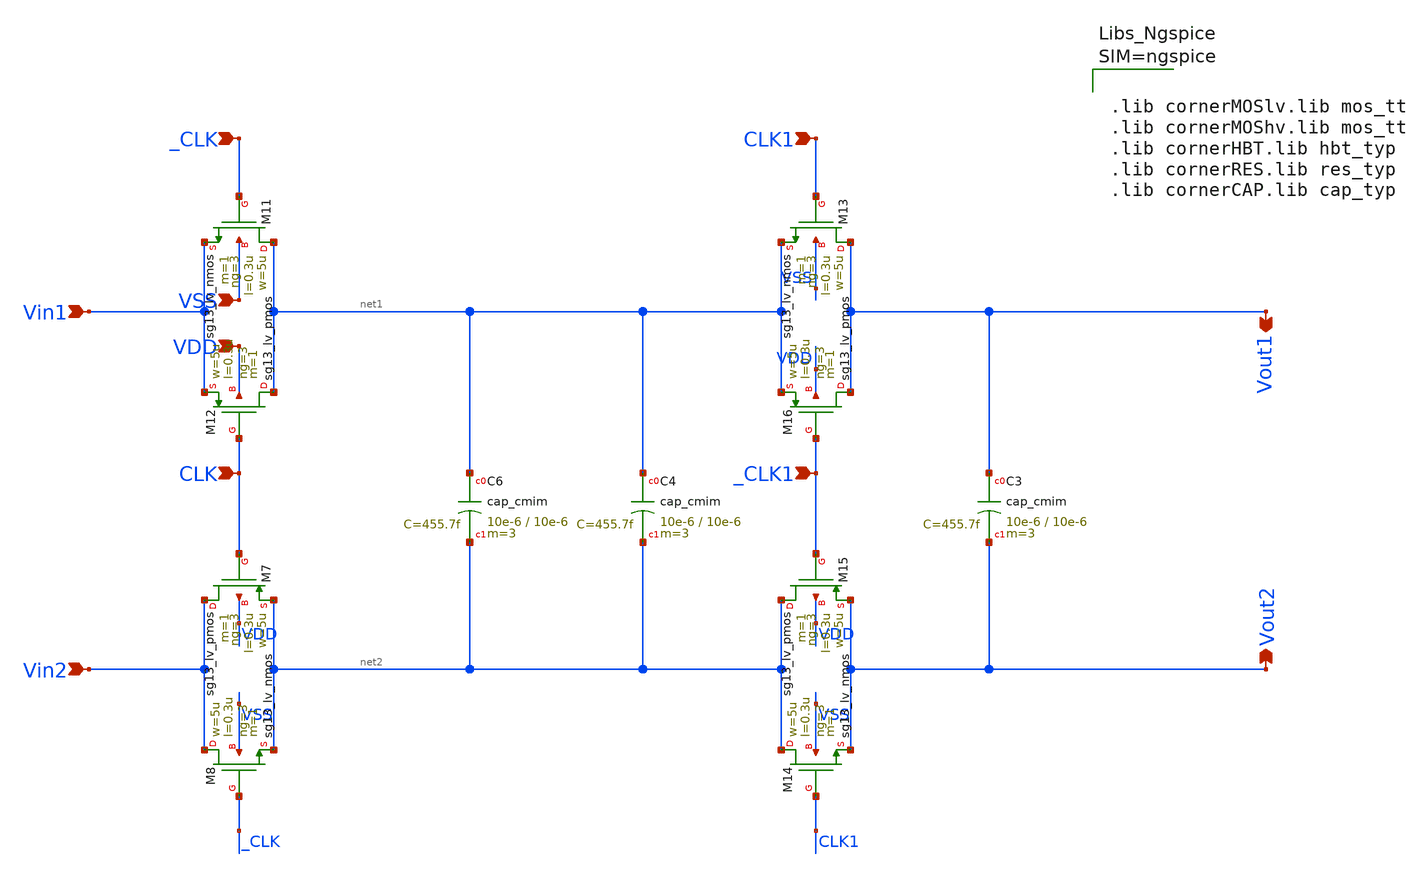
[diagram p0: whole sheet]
** sch_path: Components Progress Log/Switched-Cap Low Pass Filter/Schematic Files/lpf.sch
**.subckt lpf VSS VDD _CLK CLK Vin1 Vin2 CLK1 _CLK1 Vout1 Vout2
*.ipin VSS
*.ipin VDD
*.ipin _CLK
*.ipin CLK
*.ipin Vin1
*.ipin Vin2
*.ipin CLK1
*.ipin _CLK1
*.opin Vout1
*.opin Vout2
XC3 Vout1 Vout2 cap_cmim w=10e-6 l=10e-6 m=3 mm_ok=1
XC4 net1 net2 cap_cmim w=10e-6 l=10e-6 m=3 mm_ok=1
XC6 net1 net2 cap_cmim w=10e-6 l=10e-6 m=3 mm_ok=1
XM7 Vin2 CLK net2 VDD sg13_lv_pmos w=5u l=0.3u ng=3 m=1 mm_ok=1
XM8 Vin2 _CLK net2 VSS sg13_lv_nmos w=5u l=0.3u ng=3 m=1 mm_ok=1
XM11 net1 _CLK Vin1 VSS sg13_lv_nmos w=5u l=0.3u ng=3 m=1 mm_ok=1
XM12 net1 CLK Vin1 VDD sg13_lv_pmos w=5u l=0.3u ng=3 m=1 mm_ok=1
XM13 Vout1 CLK1 net1 VSS sg13_lv_nmos w=5u l=0.3u ng=3 m=1 mm_ok=1
XM14 net2 CLK1 Vout2 VSS sg13_lv_nmos w=5u l=0.3u ng=3 m=1 mm_ok=1
XM15 net2 _CLK1 Vout2 VDD sg13_lv_pmos w=5u l=0.3u ng=3 m=1 mm_ok=1
XM16 Vout1 _CLK1 net1 VDD sg13_lv_pmos w=5u l=0.3u ng=3 m=1 mm_ok=1
**** begin user architecture code



.lib cornerMOSlv.lib mos_tt
.lib cornerMOShv.lib mos_tt
.lib cornerHBT.lib hbt_typ
.lib cornerRES.lib res_typ
.lib cornerCAP.lib cap_typ



**** end user architecture code
**.ends
.end
